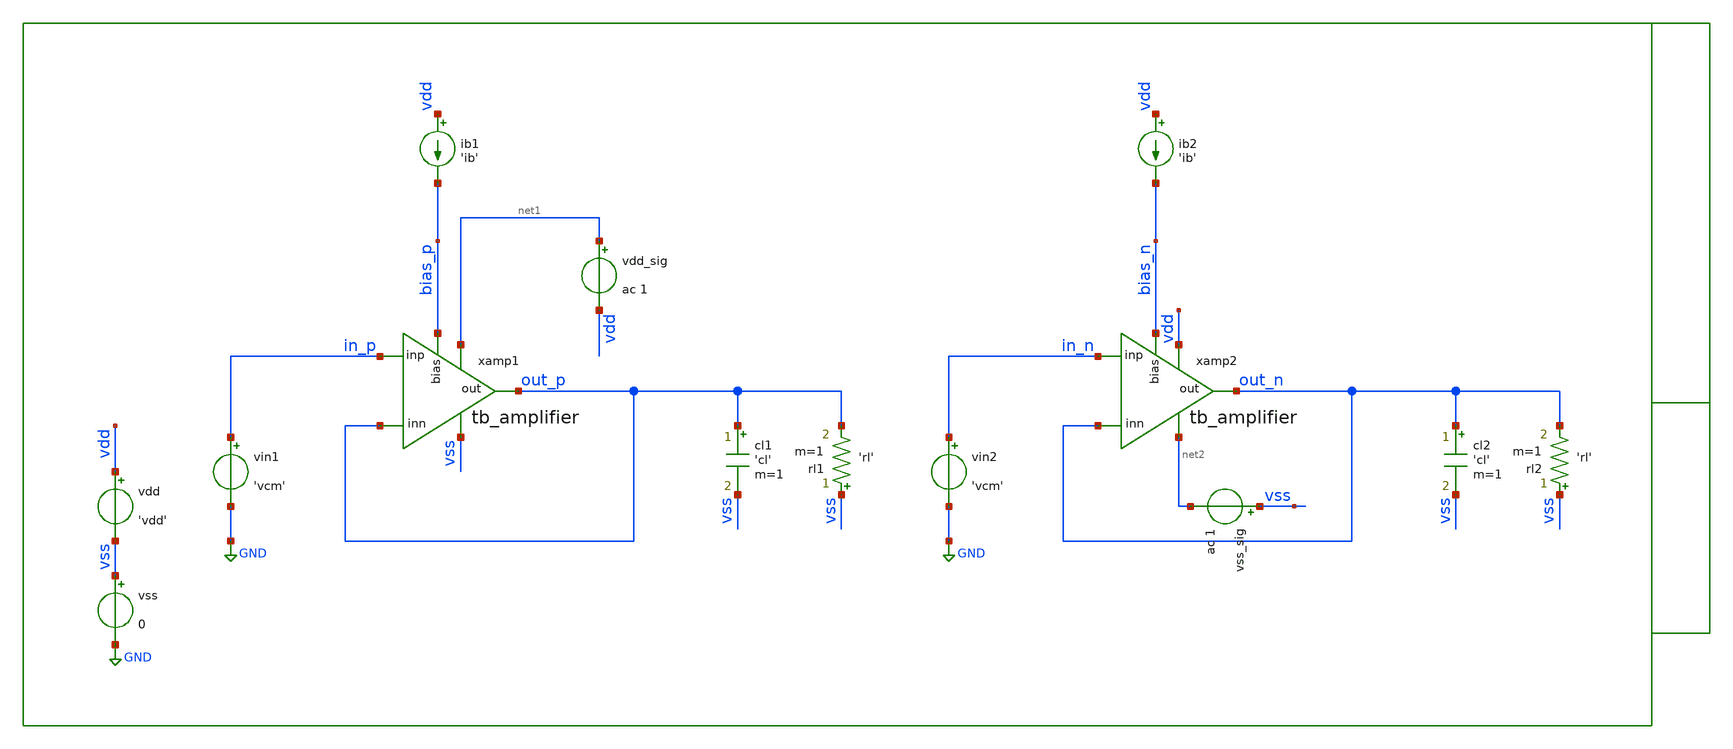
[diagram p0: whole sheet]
** sch_path: xschem/tb/testbuffer/tb_amplifier/ac_tb_amplifier_psrr.sch
**.subckt ac_tb_amplifier_psrr
vin1 in_p GND 'vcm'
cl1 out_p vss 'cl' m=1
rl1 vss out_p 'rl' m=1
ib1 vdd bias_p 'ib'
vdd_sig net1 vdd ac 1
vin2 in_n GND 'vcm'
cl2 out_n vss 'cl' m=1
rl2 vss out_n 'rl' m=1
ib2 vdd bias_n 'ib'
vss_sig vss net2 ac 1
vdd vdd vss 'vdd'
vss vss GND 0
xamp1 net1 out_p in_p out_p vss bias_p tb_amplifier
xamp2 vdd out_n in_n out_n net2 bias_n tb_amplifier
**** begin user architecture code
 * Control

.param vdd=3.3
.param vcm='vdd/2'
.param ib=5u
.param cl=10p
.param rl=10e6

.control
save all
ac dec 10 0.1 1e9
let psrr_p=(1/out_p)
let psrr_n=(1/out_n)
gnuplot p1 vdb(psrr_p)
gnuplot p2 vdb(psrr_n)
meas ac psrr_p_1    FIND vdb(psrr_p) AT=1
meas ac psrr_p_10   FIND vdb(psrr_p) AT=10
meas ac psrr_p_100  FIND vdb(psrr_p) AT=100
meas ac psrr_p_1k   FIND vdb(psrr_p) AT=1e3
meas ac psrr_p_10k  FIND vdb(psrr_p) AT=10e3
meas ac psrr_n_1    FIND vdb(psrr_n) AT=1
meas ac psrr_n_10   FIND vdb(psrr_n) AT=10
meas ac psrr_n_100  FIND vdb(psrr_n) AT=100
meas ac psrr_n_1k   FIND vdb(psrr_n) AT=1e3
meas ac psrr_n_10k  FIND vdb(psrr_n) AT=10e3
set wr_singlescale
set wr_vecnames
wrdata data.csv vdb(psrr_p) vdb(psrr_n)
.endc

 * Model Corners

.include $::CORNERS/ngspice/tt.spice
*.include $::CORNERS/ngspice/ff.spice
*.include $::CORNERS/ngspice/ss.spice
*.include $::CORNERS/ngspice/sf.spice
*.include $::CORNERS/ngspice/fs.spice

**** end user architecture code
**.ends

* expanding   symbol:  sch/testbuffer/tb_amplifier/tb_amplifier.sym # of pins=6
** sym_path: xschem/sch/testbuffer/tb_amplifier/tb_amplifier.sym
** sch_path: xschem/sch/testbuffer/tb_amplifier/tb_amplifier.sch
.subckt tb_amplifier vdd out inp inn vss bias
*.ipin inn
*.ipin inp
*.opin out
*.iopin bias
*.iopin vdd
*.iopin vss
XM3 mirr mirr vdd vdd pfet_06v0 L=4u W=16u nf=2 ad='int((nf+1)/2) * W/nf * 0.18u' as='int((nf+2)/2) * W/nf * 0.18u'
+ pd='2*int((nf+1)/2) * (W/nf + 0.18u)' ps='2*int((nf+2)/2) * (W/nf + 0.18u)' nrd='0.18u / W' nrs='0.18u / W'
+ sa=0 sb=0 sd=0 m=2 par=2
XM4 comp mirr vdd vdd pfet_06v0 L=4u W=16u nf=2 ad='int((nf+1)/2) * W/nf * 0.18u' as='int((nf+2)/2) * W/nf * 0.18u'
+ pd='2*int((nf+1)/2) * (W/nf + 0.18u)' ps='2*int((nf+2)/2) * (W/nf + 0.18u)' nrd='0.18u / W' nrs='0.18u / W'
+ sa=0 sb=0 sd=0 m=2 par=2
XM2 comp inp vcm vss nfet_06v0 L=2u W=16u nf=2 ad='int((nf+1)/2) * W/nf * 0.18u' as='int((nf+2)/2) * W/nf * 0.18u'
+ pd='2*int((nf+1)/2) * (W/nf + 0.18u)' ps='2*int((nf+2)/2) * (W/nf + 0.18u)' nrd='0.18u / W' nrs='0.18u / W'
+ sa=0 sb=0 sd=0 m=2 par=2
XM1 mirr inn vcm vss nfet_06v0 L=2u W=16u nf=2 ad='int((nf+1)/2) * W/nf * 0.18u' as='int((nf+2)/2) * W/nf * 0.18u'
+ pd='2*int((nf+1)/2) * (W/nf + 0.18u)' ps='2*int((nf+2)/2) * (W/nf + 0.18u)' nrd='0.18u / W' nrs='0.18u / W'
+ sa=0 sb=0 sd=0 m=2 par=2
XM5 vcm bias vss vss nfet_06v0 L=1u W=16u nf=2 ad='int((nf+1)/2) * W/nf * 0.18u' as='int((nf+2)/2) * W/nf * 0.18u'
+ pd='2*int((nf+1)/2) * (W/nf + 0.18u)' ps='2*int((nf+2)/2) * (W/nf + 0.18u)' nrd='0.18u / W' nrs='0.18u / W'
+ sa=0 sb=0 sd=0 m=2 par=2
XM6 out bias vss vss nfet_06v0 L=1u W=16u nf=2 ad='int((nf+1)/2) * W/nf * 0.18u' as='int((nf+2)/2) * W/nf * 0.18u'
+ pd='2*int((nf+1)/2) * (W/nf + 0.18u)' ps='2*int((nf+2)/2) * (W/nf + 0.18u)' nrd='0.18u / W' nrs='0.18u / W'
+ sa=0 sb=0 sd=0 m=12 par=12
XM7 out comp vdd vdd pfet_06v0 L=1u W=96u nf=12 ad='int((nf+1)/2) * W/nf * 0.18u' as='int((nf+2)/2) * W/nf * 0.18u'
+ pd='2*int((nf+1)/2) * (W/nf + 0.18u)' ps='2*int((nf+2)/2) * (W/nf + 0.18u)' nrd='0.18u / W' nrs='0.18u / W'
+ sa=0 sb=0 sd=0 m=1 par=1
XMB1 bias bias vss vss nfet_06v0 L=1u W=16u nf=2 ad='int((nf+1)/2) * W/nf * 0.18u' as='int((nf+2)/2) * W/nf * 0.18u'
+ pd='2*int((nf+1)/2) * (W/nf + 0.18u)' ps='2*int((nf+2)/2) * (W/nf + 0.18u)' nrd='0.18u / W' nrs='0.18u / W'
+ sa=0 sb=0 sd=0 m=2 par=2
XMB2 vbm bias vss vss nfet_06v0 L=1u W=16u nf=2 ad='int((nf+1)/2) * W/nf * 0.18u' as='int((nf+2)/2) * W/nf * 0.18u'
+ pd='2*int((nf+1)/2) * (W/nf + 0.18u)' ps='2*int((nf+2)/2) * (W/nf + 0.18u)' nrd='0.18u / W' nrs='0.18u / W'
+ sa=0 sb=0 sd=0 m=2 par=2
XMB3 vbm vbm vbt vdd pfet_06v0 L=1u W=16u nf=2 ad='int((nf+1)/2) * W/nf * 0.18u' as='int((nf+2)/2) * W/nf * 0.18u'
+ pd='2*int((nf+1)/2) * (W/nf + 0.18u)' ps='2*int((nf+2)/2) * (W/nf + 0.18u)' nrd='0.18u / W' nrs='0.18u / W'
+ sa=0 sb=0 sd=0 m=1 par=1
XMB4 vbt vbt vdd vdd pfet_06v0 L=1u W=16u nf=2 ad='int((nf+1)/2) * W/nf * 0.18u' as='int((nf+2)/2) * W/nf * 0.18u'
+ pd='2*int((nf+1)/2) * (W/nf + 0.18u)' ps='2*int((nf+2)/2) * (W/nf + 0.18u)' nrd='0.18u / W' nrs='0.18u / W'
+ sa=0 sb=0 sd=0 m=1 par=1
XRCC gc comp vdd ppolyf_u_1k_6p0 r_width=2e-6 r_length=38e-6 s=1 m=1
XMDUM1 vss vss vss vss nfet_06v0 L=2u W=16u nf=2 ad='int((nf+1)/2) * W/nf * 0.18u' as='int((nf+2)/2) * W/nf * 0.18u'
+ pd='2*int((nf+1)/2) * (W/nf + 0.18u)' ps='2*int((nf+2)/2) * (W/nf + 0.18u)' nrd='0.18u / W' nrs='0.18u / W'
+ sa=0 sb=0 sd=0 m=2 par=2
XMDUM2 vdd vdd vdd vdd pfet_06v0 L=4u W=16u nf=2 ad='int((nf+1)/2) * W/nf * 0.18u' as='int((nf+2)/2) * W/nf * 0.18u'
+ pd='2*int((nf+1)/2) * (W/nf + 0.18u)' ps='2*int((nf+2)/2) * (W/nf + 0.18u)' nrd='0.18u / W' nrs='0.18u / W'
+ sa=0 sb=0 sd=0 m=4 par=4
XC1 out gc cap_mim_2f0_m4m5_noshield c_width=30e-6 c_length=30e-6 m=1
.ends

.GLOBAL GND
.end
